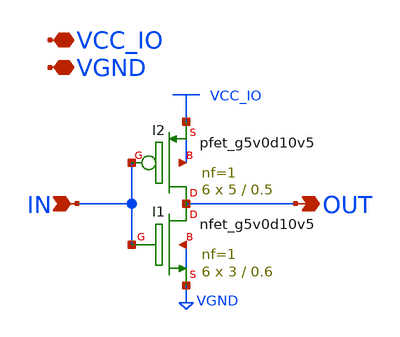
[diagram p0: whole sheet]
** sch_path: com_cclat_inv_out.sch
* Copyright 2023 David Mitchell Bailey
* Licensed under the Apache License, Version 2.0 (the "License");
* you may not use this file except in compliance with the License.
* You may obtain a copy of the License at
* https://www.apache.org/licenses/LICENSE-2.0
* Unless required by applicable law or agreed to in writing, software
* distributed under the License is distributed on an "AS IS" BASIS,
* WITHOUT WARRANTIES OR CONDITIONS OF ANY KIND, either express or implied.
* See the License for the specific language governing permissions and
* limitations under the License.
**.subckt com_cclat_inv_out IN OUT VCC_IO VGND
*.ipin IN
*.opin OUT
*.iopin VCC_IO
*.iopin VGND
XI1 OUT IN VGND VGND sky130_fd_pr__nfet_g5v0d10v5 L=0.6 W=3 nf=1 ad='int((nf+1)/2) * W/nf * 0.29' as='int((nf+2)/2) * W/nf * 0.29'
+ pd='2*int((nf+1)/2) * (W/nf + 0.29)' ps='2*int((nf+2)/2) * (W/nf + 0.29)' nrd='0.29 / W' nrs='0.29 / W'
+ sa=0 sb=0 sd=0 mult=6 m=6
XI2 OUT IN VCC_IO VCC_IO sky130_fd_pr__pfet_g5v0d10v5 L=0.5 W=5 nf=1 ad='int((nf+1)/2) * W/nf * 0.29'
+ as='int((nf+2)/2) * W/nf * 0.29' pd='2*int((nf+1)/2) * (W/nf + 0.29)' ps='2*int((nf+2)/2) * (W/nf + 0.29)'
+ nrd='0.29 / W' nrs='0.29 / W' sa=0 sb=0 sd=0 mult=6 m=6
**.ends
.end
